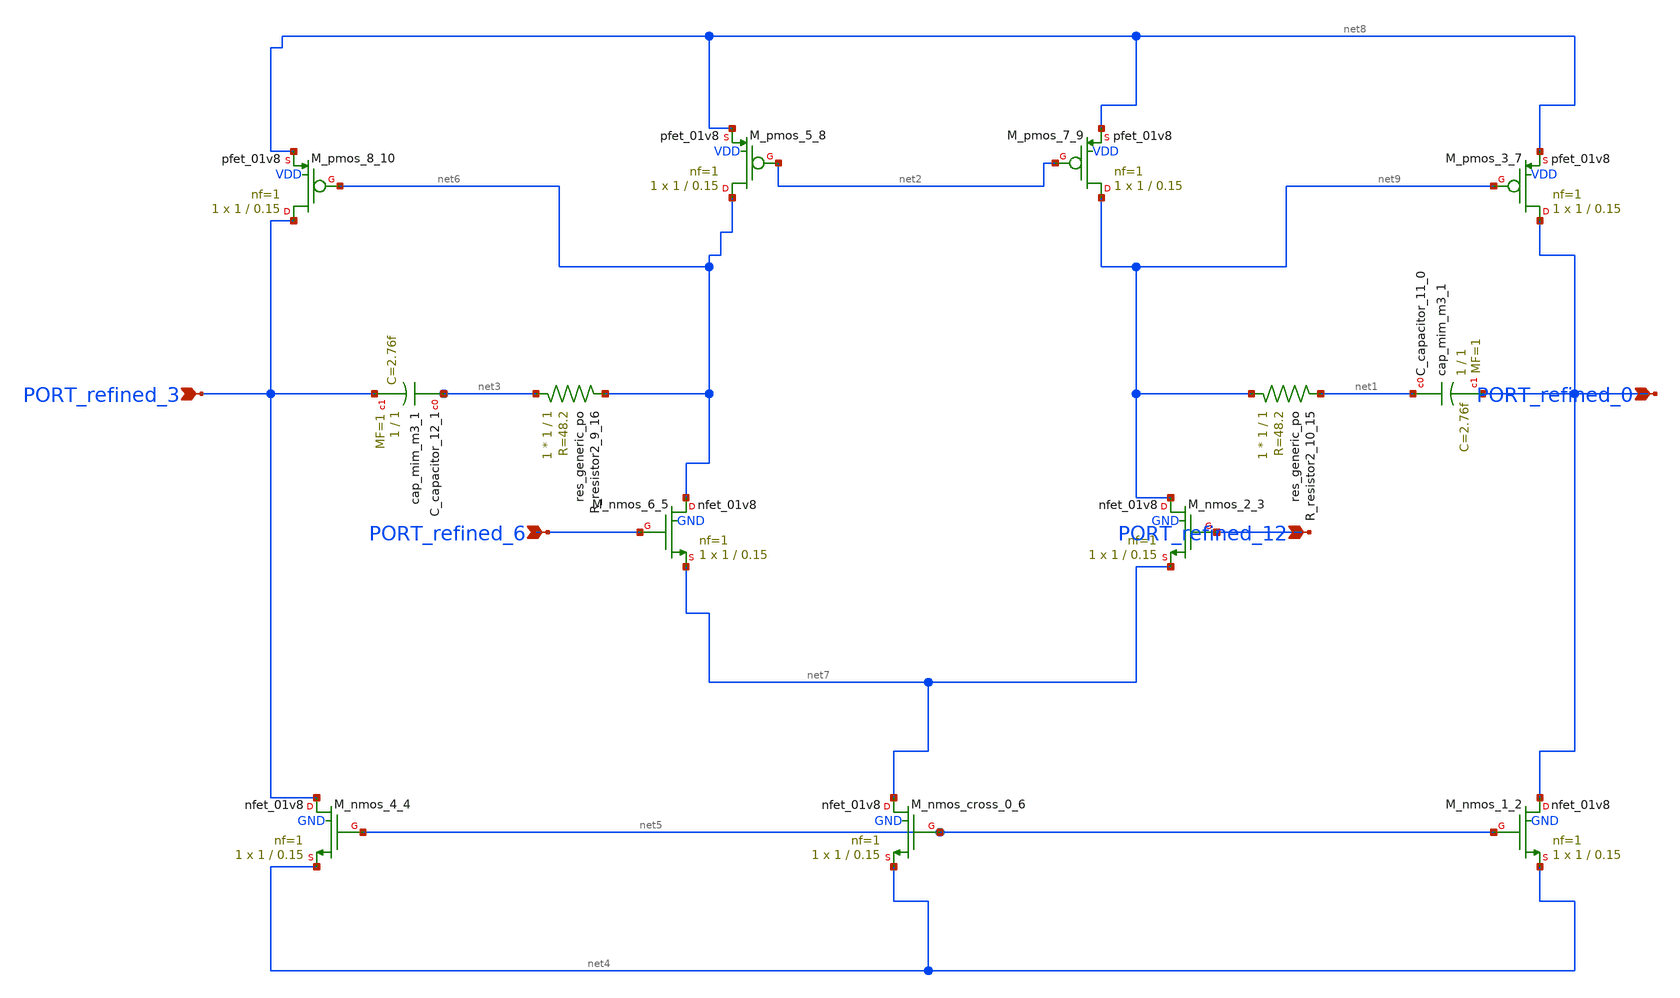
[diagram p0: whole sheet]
** sch_path: schematics/Image2Net/022.sch
**.subckt 022 PORT_refined_12 PORT_refined_6 PORT_refined_3 PORT_refined_0
*.ipin PORT_refined_12
*.ipin PORT_refined_6
*.ipin PORT_refined_3
*.ipin PORT_refined_0
XC_capacitor_11_0 net1 PORT_refined_0 sky130_fd_pr__cap_mim_m3_1 W=1 L=1 MF=1 m=1
XC_capacitor_12_1 net3 PORT_refined_3 sky130_fd_pr__cap_mim_m3_1 W=1 L=1 MF=1 m=1
XM_nmos_1_2 PORT_refined_0 net5 net4 GND sky130_fd_pr__nfet_01v8 L=0.15 W=1 nf=1 ad='int((1 + 1)/2) * 1 / 1 * 0.29'
+ as='int((1 + 2)/2) * 1 / 1 * 0.29' pd='2*int((1 + 1)/2) * (1 / 1 + 0.29)' ps='2*int((1 + 2)/2) * (1 / 1 + 0.29)'
+ nrd='0.29 / 1 ' nrs='0.29 / 1 ' sa=0 sb=0 sd=0 mult=1 m=1
XM_nmos_2_3 net9 PORT_refined_12 net7 GND sky130_fd_pr__nfet_01v8 L=0.15 W=1 nf=1 ad='int((1 + 1)/2) * 1 / 1 * 0.29'
+ as='int((1 + 2)/2) * 1 / 1 * 0.29' pd='2*int((1 + 1)/2) * (1 / 1 + 0.29)' ps='2*int((1 + 2)/2) * (1 / 1 + 0.29)'
+ nrd='0.29 / 1 ' nrs='0.29 / 1 ' sa=0 sb=0 sd=0 mult=1 m=1
XM_nmos_4_4 PORT_refined_3 net5 net4 GND sky130_fd_pr__nfet_01v8 L=0.15 W=1 nf=1 ad='int((1 + 1)/2) * 1 / 1 * 0.29'
+ as='int((1 + 2)/2) * 1 / 1 * 0.29' pd='2*int((1 + 1)/2) * (1 / 1 + 0.29)' ps='2*int((1 + 2)/2) * (1 / 1 + 0.29)'
+ nrd='0.29 / 1 ' nrs='0.29 / 1 ' sa=0 sb=0 sd=0 mult=1 m=1
XM_nmos_6_5 net6 PORT_refined_6 net7 GND sky130_fd_pr__nfet_01v8 L=0.15 W=1 nf=1 ad='int((1 + 1)/2) * 1 / 1 * 0.29'
+ as='int((1 + 2)/2) * 1 / 1 * 0.29' pd='2*int((1 + 1)/2) * (1 / 1 + 0.29)' ps='2*int((1 + 2)/2) * (1 / 1 + 0.29)'
+ nrd='0.29 / 1 ' nrs='0.29 / 1 ' sa=0 sb=0 sd=0 mult=1 m=1
XM_nmos_cross_0_6 net7 net5 net4 GND sky130_fd_pr__nfet_01v8 L=0.15 W=1 nf=1 ad='int((1 + 1)/2) * 1 / 1 * 0.29'
+ as='int((1 + 2)/2) * 1 / 1 * 0.29' pd='2*int((1 + 1)/2) * (1 / 1 + 0.29)' ps='2*int((1 + 2)/2) * (1 / 1 + 0.29)'
+ nrd='0.29 / 1 ' nrs='0.29 / 1 ' sa=0 sb=0 sd=0 mult=1 m=1
XM_pmos_3_7 PORT_refined_0 net9 net8 VDD sky130_fd_pr__pfet_01v8 L=0.15 W=1 nf=1 ad='int((1 + 1)/2) * 1 / 1 * 0.29'
+ as='int((1 + 2)/2) * 1 / 1 * 0.29' pd='2*int((1 + 1)/2) * (1 / 1 + 0.29)' ps='2*int((1 + 2)/2) * (1 / 1 + 0.29)'
+ nrd='0.29 / 1 ' nrs='0.29 / 1 ' sa=0 sb=0 sd=0 mult=1 m=1
XM_pmos_5_8 net6 net2 net8 VDD sky130_fd_pr__pfet_01v8 L=0.15 W=1 nf=1 ad='int((1 + 1)/2) * 1 / 1 * 0.29'
+ as='int((1 + 2)/2) * 1 / 1 * 0.29' pd='2*int((1 + 1)/2) * (1 / 1 + 0.29)' ps='2*int((1 + 2)/2) * (1 / 1 + 0.29)'
+ nrd='0.29 / 1 ' nrs='0.29 / 1 ' sa=0 sb=0 sd=0 mult=1 m=1
XM_pmos_7_9 net9 net2 net8 VDD sky130_fd_pr__pfet_01v8 L=0.15 W=1 nf=1 ad='int((1 + 1)/2) * 1 / 1 * 0.29'
+ as='int((1 + 2)/2) * 1 / 1 * 0.29' pd='2*int((1 + 1)/2) * (1 / 1 + 0.29)' ps='2*int((1 + 2)/2) * (1 / 1 + 0.29)'
+ nrd='0.29 / 1 ' nrs='0.29 / 1 ' sa=0 sb=0 sd=0 mult=1 m=1
XM_pmos_8_10 PORT_refined_3 net6 net8 VDD sky130_fd_pr__pfet_01v8 L=0.15 W=1 nf=1 ad='int((1 + 1)/2) * 1 / 1 * 0.29'
+ as='int((1 + 2)/2) * 1 / 1 * 0.29' pd='2*int((1 + 1)/2) * (1 / 1 + 0.29)' ps='2*int((1 + 2)/2) * (1 / 1 + 0.29)'
+ nrd='0.29 / 1 ' nrs='0.29 / 1 ' sa=0 sb=0 sd=0 mult=1 m=1
XR_resistor2_10_15 net9 net1 sky130_fd_pr__res_generic_po W=1 L=1 m=1
XR_resistor2_9_16 net3 net6 sky130_fd_pr__res_generic_po W=1 L=1 m=1
**.ends
.end
